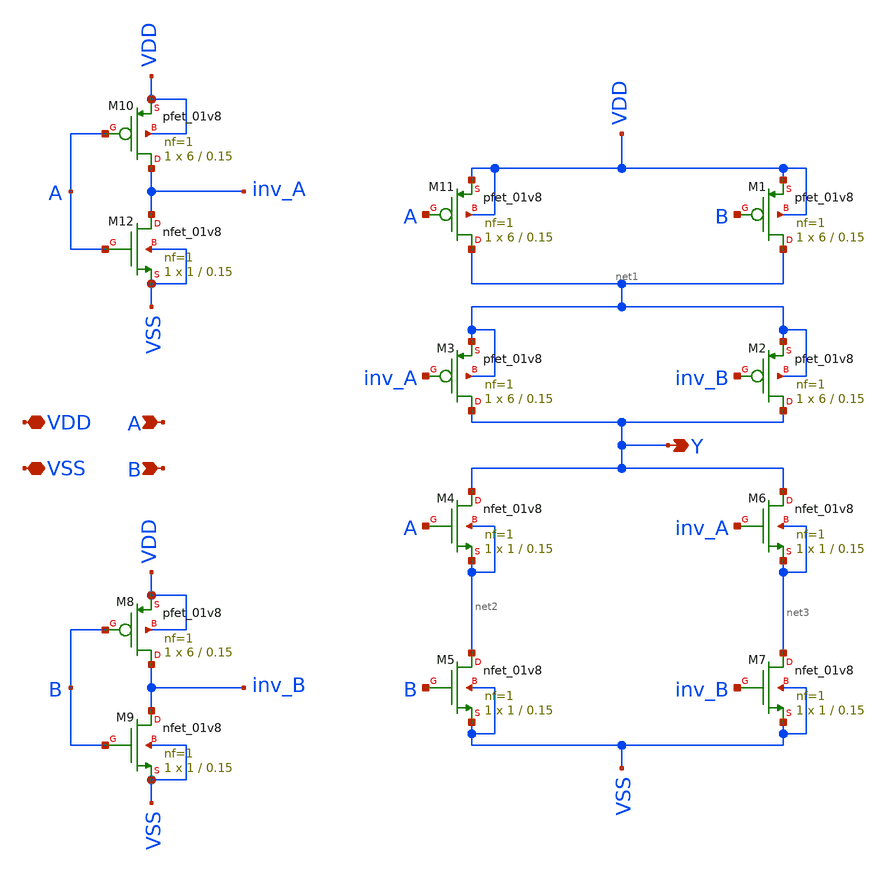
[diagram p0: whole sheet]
** sch_path: design/xor_with_fo4/xor2.sch
**.subckt xor2 Y A VDD VSS B
*.opin Y
*.ipin A
*.iopin VDD
*.iopin VSS
*.ipin B
XM11 net1 A VDD VDD sky130_fd_pr__pfet_01v8 L=0.15 W=6 nf=1 ad='int((nf+1)/2) * W/nf * 0.29' as='int((nf+2)/2) * W/nf * 0.29'
+ pd='2*int((nf+1)/2) * (W/nf + 0.29)' ps='2*int((nf+2)/2) * (W/nf + 0.29)' nrd='0.29 / W' nrs='0.29 / W'
+ sa=0 sb=0 sd=0 mult=1 m=1
XM1 net1 B VDD VDD sky130_fd_pr__pfet_01v8 L=0.15 W=6 nf=1 ad='int((nf+1)/2) * W/nf * 0.29' as='int((nf+2)/2) * W/nf * 0.29'
+ pd='2*int((nf+1)/2) * (W/nf + 0.29)' ps='2*int((nf+2)/2) * (W/nf + 0.29)' nrd='0.29 / W' nrs='0.29 / W'
+ sa=0 sb=0 sd=0 mult=1 m=1
XM2 Y inv_B net1 net1 sky130_fd_pr__pfet_01v8 L=0.15 W=6 nf=1 ad='int((nf+1)/2) * W/nf * 0.29' as='int((nf+2)/2) * W/nf * 0.29'
+ pd='2*int((nf+1)/2) * (W/nf + 0.29)' ps='2*int((nf+2)/2) * (W/nf + 0.29)' nrd='0.29 / W' nrs='0.29 / W'
+ sa=0 sb=0 sd=0 mult=1 m=1
XM3 Y inv_A net1 net1 sky130_fd_pr__pfet_01v8 L=0.15 W=6 nf=1 ad='int((nf+1)/2) * W/nf * 0.29' as='int((nf+2)/2) * W/nf * 0.29'
+ pd='2*int((nf+1)/2) * (W/nf + 0.29)' ps='2*int((nf+2)/2) * (W/nf + 0.29)' nrd='0.29 / W' nrs='0.29 / W'
+ sa=0 sb=0 sd=0 mult=1 m=1
XM4 Y A net2 net2 sky130_fd_pr__nfet_01v8 L=0.15 W=1 nf=1 ad='int((1 + 1)/2) * 1 / 1 * 0.29' as='int((1 + 2)/2) * 1 / 1 * 0.29'
+ pd='2*int((1 + 1)/2) * (1 / 1 + 0.29)' ps='2*int((1 + 2)/2) * (1 / 1 + 0.29)' nrd='0.29 / 1 ' nrs='0.29 / 1 '
+ sa=0 sb=0 sd=0 mult=1 m=1
XM5 net2 B VSS VSS sky130_fd_pr__nfet_01v8 L=0.15 W=1 nf=1 ad='int((1 + 1)/2) * 1 / 1 * 0.29' as='int((1 + 2)/2) * 1 / 1 * 0.29'
+ pd='2*int((1 + 1)/2) * (1 / 1 + 0.29)' ps='2*int((1 + 2)/2) * (1 / 1 + 0.29)' nrd='0.29 / 1 ' nrs='0.29 / 1 '
+ sa=0 sb=0 sd=0 mult=1 m=1
XM6 Y inv_A net3 net3 sky130_fd_pr__nfet_01v8 L=0.15 W=1 nf=1 ad='int((1 + 1)/2) * 1 / 1 * 0.29' as='int((1 + 2)/2) * 1 / 1 * 0.29'
+ pd='2*int((1 + 1)/2) * (1 / 1 + 0.29)' ps='2*int((1 + 2)/2) * (1 / 1 + 0.29)' nrd='0.29 / 1 ' nrs='0.29 / 1 '
+ sa=0 sb=0 sd=0 mult=1 m=1
XM7 net3 inv_B VSS VSS sky130_fd_pr__nfet_01v8 L=0.15 W=1 nf=1 ad='int((1 + 1)/2) * 1 / 1 * 0.29' as='int((1 + 2)/2) * 1 / 1 * 0.29'
+ pd='2*int((1 + 1)/2) * (1 / 1 + 0.29)' ps='2*int((1 + 2)/2) * (1 / 1 + 0.29)' nrd='0.29 / 1 ' nrs='0.29 / 1 '
+ sa=0 sb=0 sd=0 mult=1 m=1
XM8 inv_B B VDD VDD sky130_fd_pr__pfet_01v8 L=0.15 W=6 nf=1 ad='int((nf+1)/2) * W/nf * 0.29' as='int((nf+2)/2) * W/nf * 0.29'
+ pd='2*int((nf+1)/2) * (W/nf + 0.29)' ps='2*int((nf+2)/2) * (W/nf + 0.29)' nrd='0.29 / W' nrs='0.29 / W'
+ sa=0 sb=0 sd=0 mult=1 m=1
XM9 inv_B B VSS VSS sky130_fd_pr__nfet_01v8 L=0.15 W=1 nf=1 ad='int((1 + 1)/2) * 1 / 1 * 0.29' as='int((1 + 2)/2) * 1 / 1 * 0.29'
+ pd='2*int((1 + 1)/2) * (1 / 1 + 0.29)' ps='2*int((1 + 2)/2) * (1 / 1 + 0.29)' nrd='0.29 / 1 ' nrs='0.29 / 1 '
+ sa=0 sb=0 sd=0 mult=1 m=1
XM10 inv_A A VDD VDD sky130_fd_pr__pfet_01v8 L=0.15 W=6 nf=1 ad='int((nf+1)/2) * W/nf * 0.29' as='int((nf+2)/2) * W/nf * 0.29'
+ pd='2*int((nf+1)/2) * (W/nf + 0.29)' ps='2*int((nf+2)/2) * (W/nf + 0.29)' nrd='0.29 / W' nrs='0.29 / W'
+ sa=0 sb=0 sd=0 mult=1 m=1
XM12 inv_A A VSS VSS sky130_fd_pr__nfet_01v8 L=0.15 W=1 nf=1 ad='int((1 + 1)/2) * 1 / 1 * 0.29' as='int((1 + 2)/2) * 1 / 1 * 0.29'
+ pd='2*int((1 + 1)/2) * (1 / 1 + 0.29)' ps='2*int((1 + 2)/2) * (1 / 1 + 0.29)' nrd='0.29 / 1 ' nrs='0.29 / 1 '
+ sa=0 sb=0 sd=0 mult=1 m=1
**.ends
.end
